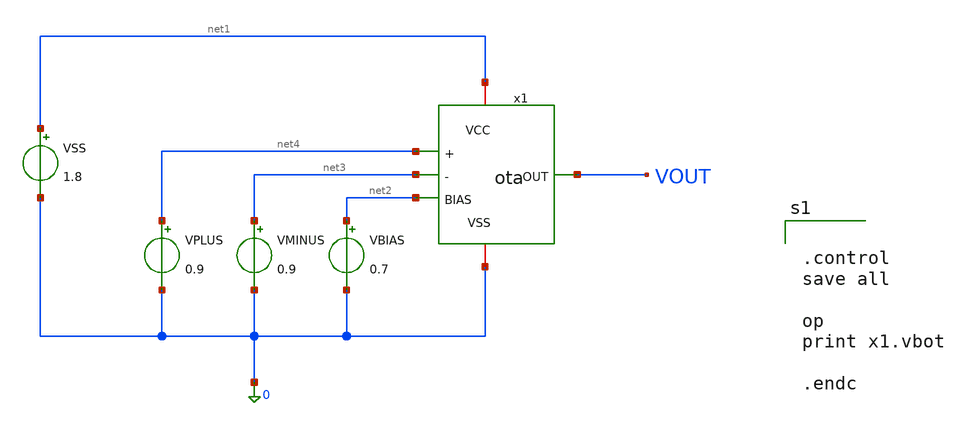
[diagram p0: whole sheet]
** sch_path: schem/ota/ota_tb.sch
**.subckt ota_tb
VSS net1 0 1.8
VBIAS net2 0 0.7
VMINUS net3 0 0.9
VPLUS net4 0 0.9
x1 net1 VOUT 0 net2 net4 net3 ota
**** begin user architecture code

** opencircuitdesign pdks install
.lib $::SKYWATER_MODELS/sky130.lib.spice tt



.control
save all

op
print x1.vbot

.endc


**** end user architecture code
**.ends

* expanding   symbol:  ota.sym # of pins=6
** sym_path: schem/ota/ota.sym
** sch_path: schem/ota/ota.sch
.subckt ota VCC OUT VSS BIAS + -
*.ipin BIAS
*.ipin +
*.ipin -
*.opin OUT
*.iopin VCC
*.iopin VSS
XM1 VSRC + VBOT VSS sky130_fd_pr__nfet_01v8 L=0.5 W=1 nf=1 ad='int((1 + 1)/2) * 1 / 1 * 0.29' as='int((1 + 2)/2) * 1 / 1 * 0.29'
+ pd='2*int((1 + 1)/2) * (1 / 1 + 0.29)' ps='2*int((1 + 2)/2) * (1 / 1 + 0.29)' nrd='0.29 / 1 ' nrs='0.29 / 1 '
+ sa=0 sb=0 sd=0 mult=1 m=1
XM2 OUT - VBOT VSS sky130_fd_pr__nfet_01v8 L=0.5 W=1 nf=1 ad='int((1 + 1)/2) * 1 / 1 * 0.29' as='int((1 + 2)/2) * 1 / 1 * 0.29'
+ pd='2*int((1 + 1)/2) * (1 / 1 + 0.29)' ps='2*int((1 + 2)/2) * (1 / 1 + 0.29)' nrd='0.29 / 1 ' nrs='0.29 / 1 '
+ sa=0 sb=0 sd=0 mult=1 m=1
XM3 VSRC VSRC VCC VCC sky130_fd_pr__pfet_01v8_lvt L=0.5 W=2 nf=1 ad='int((1 + 1)/2) * 2 / 1 * 0.29' as='int((1 + 2)/2) * 2 / 1 * 0.29'
+ pd='2*int((1 + 1)/2) * (2 / 1 + 0.29)' ps='2*int((1 + 2)/2) * (2 / 1 + 0.29)' nrd='0.29 / 2 ' nrs='0.29 / 2 '
+ sa=0 sb=0 sd=0 mult=1 m=1
XM4 OUT VSRC VCC VCC sky130_fd_pr__pfet_01v8_lvt L=0.5 W=2 nf=1 ad='int((1 + 1)/2) * 2 / 1 * 0.29' as='int((1 + 2)/2) * 2 / 1 * 0.29'
+ pd='2*int((1 + 1)/2) * (2 / 1 + 0.29)' ps='2*int((1 + 2)/2) * (2 / 1 + 0.29)' nrd='0.29 / 2 ' nrs='0.29 / 2 '
+ sa=0 sb=0 sd=0 mult=1 m=1
XM5 VBOT BIAS VSS VSS sky130_fd_pr__nfet_01v8 L=0.5 W=1 nf=1 ad='int((1 + 1)/2) * 1 / 1 * 0.29' as='int((1 + 2)/2) * 1 / 1 * 0.29'
+ pd='2*int((1 + 1)/2) * (1 / 1 + 0.29)' ps='2*int((1 + 2)/2) * (1 / 1 + 0.29)' nrd='0.29 / 1 ' nrs='0.29 / 1 '
+ sa=0 sb=0 sd=0 mult=1 m=1
.ends

.end
